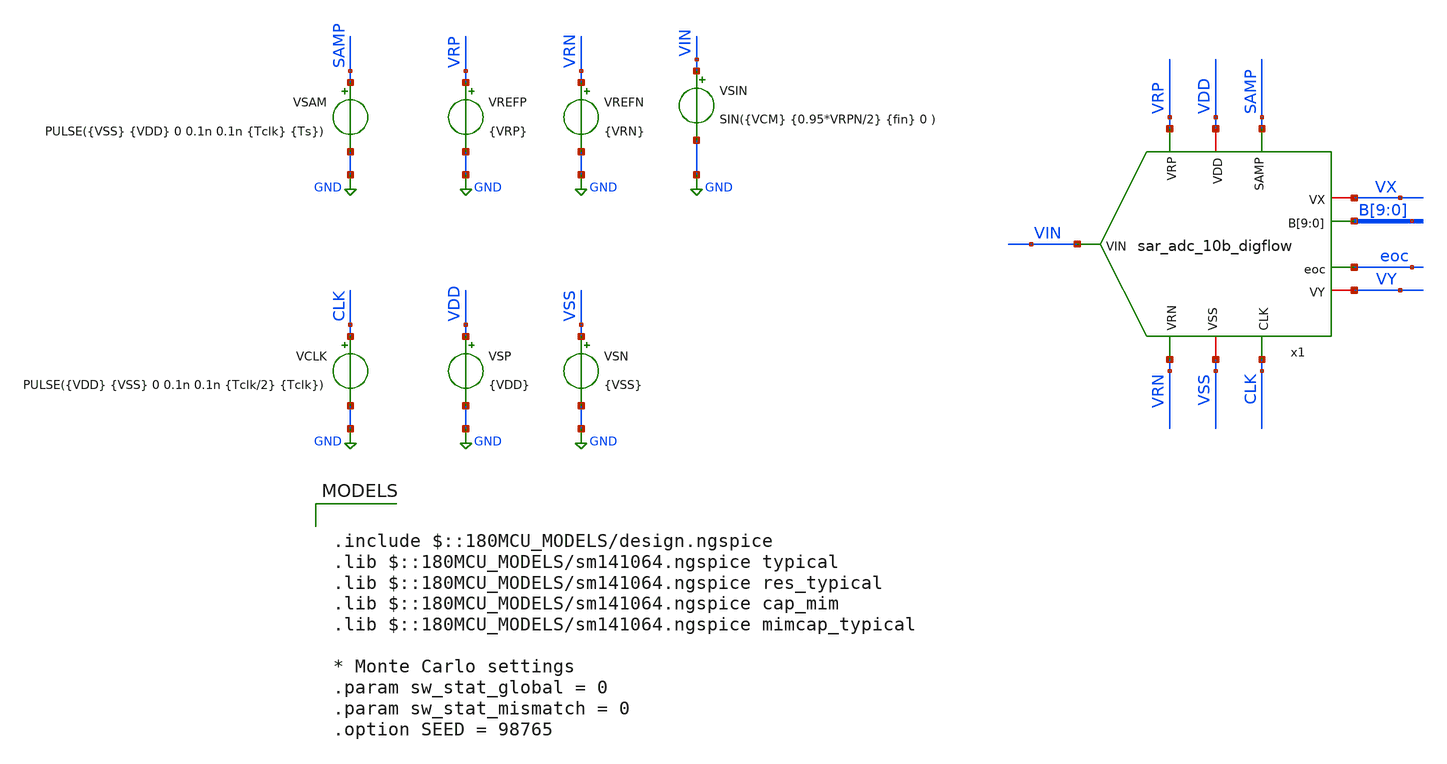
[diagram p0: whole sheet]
** sch_path: designs/sar_adc/top/sar_adc_10b_digflow/xschem/tb_sar_adc_10b_digflow.sch
**.subckt tb_sar_adc_10b_digflow
VSP VDD GND {VDD}
VSN VSS GND {VSS}
VREFP VRP GND {VRP}
VREFN VRN GND {VRN}
VSIN VIN GND SIN({VCM} {0.95*VRPN/2} {fin} 0 )
VSAM SAMP GND PULSE({VSS} {VDD} 0 0.1n 0.1n {Tclk} {Ts})
VCLK CLK GND PULSE({VDD} {VSS} 0 0.1n 0.1n {Tclk/2} {Tclk})
x1 VIN VDD VSS VRP VX B[9] B[8] B[7] B[6] B[5] B[4] B[3] B[2] B[1] B[0] SAMP CLK VY VRN eoc
+ sar_adc_10b_digflow
**** begin user architecture code


.temp 27

* Voltages
.param VDD = 3.3
.param VSS = 0
.param VRP = 2.1
.param VRN = 1.2
.param VRPN = VRP-VRN
.param VCM = (VRP+VRN)/2

* Input parameters
.param Fs = 5Meg
.param Ns = 64
.param Nc = 31
.param fin = Nc/Ns*Fs

* Sampling clock
.param Ts = 1/Fs
.param Tclk = 1/(Fs*12)

.control

* Local variables for .control
let Fs = 5Meg
let Ns = 0
let Nspare = 5
let VRP = 2.1
let VRN = 1.2
let VRPN = VRP - VRN
let VDD = 3.3

let tstep = 1/(Fs*12*200)
let tstop = (Ns + Nspare)/Fs

* Save main signals
save V(VIN) V(VX) V(VY) "B[9]" "B[8]" "B[7]" "B[6]" "B[5]" "B[4]" "B[3]" "B[2]" "B[1]" "B[0]"
+ V(xADC.COMP) I(VSP) I(VREFP) I(VREFN) v(samp) v(clk)
*save all

* Transient simulation
tran $&tstep $&tstop

* Output waveforms
linearize
let vin = v(vin)
let samp = v(samp)
let clk = v(clk)
let vxy = V(VX)-V(VY)
let vin2 = v(vin)*2 - (VRP + VRN)
let dout = ("B[9]"*1/2 + "B[8]"*1/4 +  "B[7]"*1/8 + "B[6]"*1/16 +  "B[5]"*1/32 + "B[4]"*1/64 +
+  "B[3]"*1/128 + "B[2]"*1/256 +  "B[1]"*1/512 + "B[0]"*1/1024)
let dout2 = dout*2*VRPN/vdd - vrpn

* Power measurement
* REFERENCE:
let P_REF = -1*VRP*i(VREFP) - 1*VRN*i(VREFN)
meas tran P_REF_avg AVG P_REF from=tstep to=tstop

* SUPPLY:
let P_VDD = -1*VDD*i(VSP)
meas tran P_VDD_avg AVG P_VDD from=tstep to=tstop
let P_T_avg = P_REF_avg + P_VDD_avg

* Print outputs
echo ============================================================
echo POWER_AND_RESISTANCE
echo ============================================================

echo REF POWER = $&P_REF_avg W
echo VDD POWER = $&P_VDD_avg W
echo TOTAL POWER = $&P_T_avg W

* export waveforms
wrdata tb_sar_adc_10b_digflow.csv v(VIN) v(VX) v(VY) dout P_REF P_VDD

 * Plots
*plot V(VX) V(VY)
*plot V(VIN) V(VRP) V(VRN)
*plot V(CLK) V(SAMP)
*plot V(xADC.COMP)
*plot vxy dout
*plot vxy V(VIN)
*plot dout V(VIN)
plot dout2 vin2 vxy

.endc



.include $::180MCU_MODELS/design.ngspice
.lib $::180MCU_MODELS/sm141064.ngspice typical
.lib $::180MCU_MODELS/sm141064.ngspice res_typical
.lib $::180MCU_MODELS/sm141064.ngspice cap_mim
.lib $::180MCU_MODELS/sm141064.ngspice mimcap_typical

* Monte Carlo settings
.param sw_stat_global = 0
.param sw_stat_mismatch = 0
.option SEED = 98765

**** end user architecture code
**.ends
.GLOBAL GND
.end
